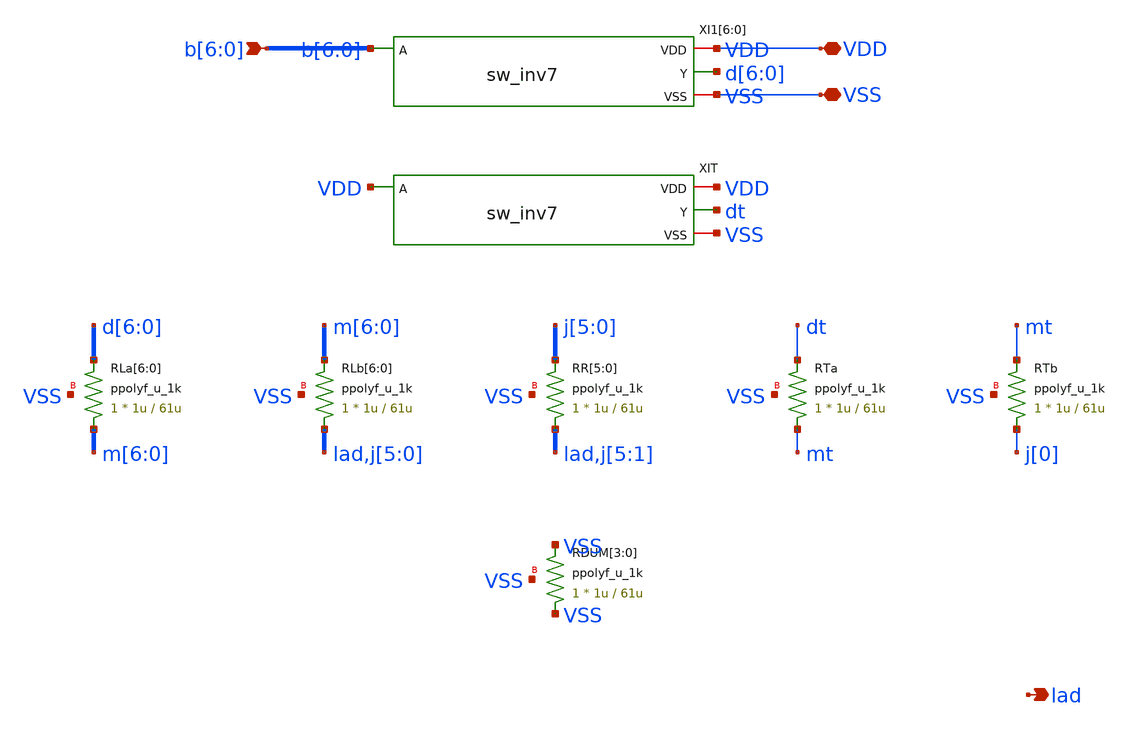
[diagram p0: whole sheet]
** sch_path: xschem/pll_dac/r2r7.sch
**.subckt r2r7 VDD VSS b[6],b[5],b[4],b[3],b[2],b[1],b[0] lad
*.iopin VDD
*.iopin VSS
*.ipin b[6],b[5],b[4],b[3],b[2],b[1],b[0]
*.opin lad
XRLa[6] m[6] d[6] VSS ppolyf_u_1k r_width=1u r_length=61u m=1
XRLa[5] m[5] d[5] VSS ppolyf_u_1k r_width=1u r_length=61u m=1
XRLa[4] m[4] d[4] VSS ppolyf_u_1k r_width=1u r_length=61u m=1
XRLa[3] m[3] d[3] VSS ppolyf_u_1k r_width=1u r_length=61u m=1
XRLa[2] m[2] d[2] VSS ppolyf_u_1k r_width=1u r_length=61u m=1
XRLa[1] m[1] d[1] VSS ppolyf_u_1k r_width=1u r_length=61u m=1
XRLa[0] m[0] d[0] VSS ppolyf_u_1k r_width=1u r_length=61u m=1
XRLb[6] lad m[6] VSS ppolyf_u_1k r_width=1u r_length=61u m=1
XRLb[5] j[5] m[5] VSS ppolyf_u_1k r_width=1u r_length=61u m=1
XRLb[4] j[4] m[4] VSS ppolyf_u_1k r_width=1u r_length=61u m=1
XRLb[3] j[3] m[3] VSS ppolyf_u_1k r_width=1u r_length=61u m=1
XRLb[2] j[2] m[2] VSS ppolyf_u_1k r_width=1u r_length=61u m=1
XRLb[1] j[1] m[1] VSS ppolyf_u_1k r_width=1u r_length=61u m=1
XRLb[0] j[0] m[0] VSS ppolyf_u_1k r_width=1u r_length=61u m=1
XRR[5] lad j[5] VSS ppolyf_u_1k r_width=1u r_length=61u m=1
XRR[4] j[5] j[4] VSS ppolyf_u_1k r_width=1u r_length=61u m=1
XRR[3] j[4] j[3] VSS ppolyf_u_1k r_width=1u r_length=61u m=1
XRR[2] j[3] j[2] VSS ppolyf_u_1k r_width=1u r_length=61u m=1
XRR[1] j[2] j[1] VSS ppolyf_u_1k r_width=1u r_length=61u m=1
XRR[0] j[1] j[0] VSS ppolyf_u_1k r_width=1u r_length=61u m=1
XRTa mt dt VSS ppolyf_u_1k r_width=1u r_length=61u m=1
XRTb j[0] mt VSS ppolyf_u_1k r_width=1u r_length=61u m=1
XRDUM[3] VSS VSS VSS ppolyf_u_1k r_width=1u r_length=61u m=1
XRDUM[2] VSS VSS VSS ppolyf_u_1k r_width=1u r_length=61u m=1
XRDUM[1] VSS VSS VSS ppolyf_u_1k r_width=1u r_length=61u m=1
XRDUM[0] VSS VSS VSS ppolyf_u_1k r_width=1u r_length=61u m=1
XI1[6] VDD b[6] d[6] VSS sw_inv7
XI1[5] VDD b[5] d[5] VSS sw_inv7
XI1[4] VDD b[4] d[4] VSS sw_inv7
XI1[3] VDD b[3] d[3] VSS sw_inv7
XI1[2] VDD b[2] d[2] VSS sw_inv7
XI1[1] VDD b[1] d[1] VSS sw_inv7
XI1[0] VDD b[0] d[0] VSS sw_inv7
XIT VDD VDD dt VSS sw_inv7
**.ends
.end
